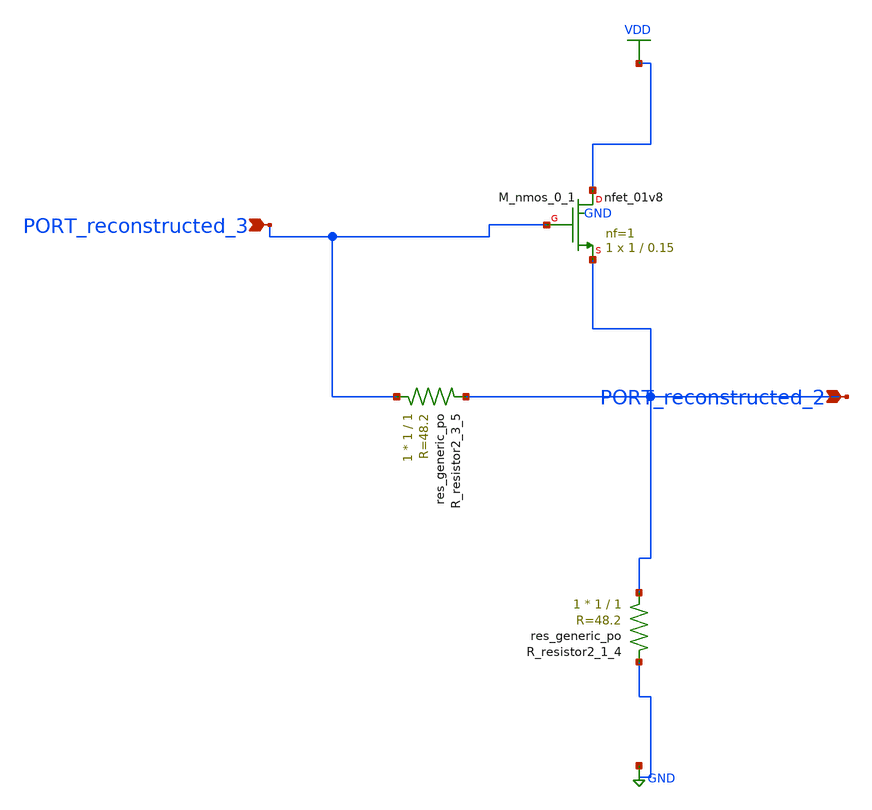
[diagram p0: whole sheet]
** sch_path: schematics/AMSNet/150.sch
**.subckt 150 PORT_reconstructed_2 PORT_reconstructed_3
*.ipin PORT_reconstructed_2
*.ipin PORT_reconstructed_3
XM_nmos_0_1 VDD PORT_reconstructed_3 PORT_reconstructed_2 GND sky130_fd_pr__nfet_01v8 L=0.15 W=1 nf=1
+ ad='int((1 + 1)/2) * 1 / 1 * 0.29' as='int((1 + 2)/2) * 1 / 1 * 0.29' pd='2*int((1 + 1)/2) * (1 / 1 + 0.29)'
+ ps='2*int((1 + 2)/2) * (1 / 1 + 0.29)' nrd='0.29 / 1 ' nrs='0.29 / 1 ' sa=0 sb=0 sd=0 mult=1 m=1
XR_resistor2_1_4 PORT_reconstructed_2 GND sky130_fd_pr__res_generic_po W=1 L=1 m=1
XR_resistor2_3_5 PORT_reconstructed_3 PORT_reconstructed_2 sky130_fd_pr__res_generic_po W=1 L=1 m=1
**.ends
.GLOBAL GND
.GLOBAL VDD
.end
